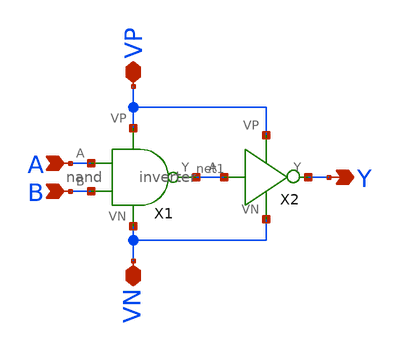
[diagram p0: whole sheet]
** sch_path: mp1/and/and.sch
**.subckt and A B VP VN Y
*.ipin A
*.ipin B
*.iopin VP
*.iopin VN
*.opin Y
X2 net1 Y VP VN inverter
X1 A B net1 VP VN nand
**.ends

* expanding   symbol:  /home/madvlsi/Documents/mp1/inverter/inverter.sym # of pins=4
** sym_path: mp1/inverter/inverter.sym
** sch_path: mp1/inverter/inverter.sch
.subckt inverter A Y VP VN
*.ipin A
*.iopin VP
*.iopin VN
*.opin Y
XM1 Y A VN VN sky130_fd_pr__nfet_01v8 L=0.15 W=1 nf=1 ad='int((nf+1)/2) * W/nf * 0.29' as='int((nf+2)/2) * W/nf * 0.29'
+ pd='2*int((nf+1)/2) * (W/nf + 0.29)' ps='2*int((nf+2)/2) * (W/nf + 0.29)' nrd='0.29 / W' nrs='0.29 / W'
+ sa=0 sb=0 sd=0 mult=1 m=1
XM2 Y A VP VP sky130_fd_pr__pfet_01v8 L=0.15 W=1 nf=1 ad='int((nf+1)/2) * W/nf * 0.29' as='int((nf+2)/2) * W/nf * 0.29'
+ pd='2*int((nf+1)/2) * (W/nf + 0.29)' ps='2*int((nf+2)/2) * (W/nf + 0.29)' nrd='0.29 / W' nrs='0.29 / W'
+ sa=0 sb=0 sd=0 mult=1 m=1
.ends


* expanding   symbol:  /home/madvlsi/Documents/mp1/nand/nand.sym # of pins=5
** sym_path: mp1/nand/nand.sym
** sch_path: mp1/nand/nand.sch
.subckt nand A B Y VP VN
*.ipin A
*.ipin B
*.opin Y
*.iopin VP
*.iopin VN
XM1 Y A VP VP sky130_fd_pr__pfet_01v8 L=0.15 W=1 nf=1 ad='int((nf+1)/2) * W/nf * 0.29' as='int((nf+2)/2) * W/nf * 0.29'
+ pd='2*int((nf+1)/2) * (W/nf + 0.29)' ps='2*int((nf+2)/2) * (W/nf + 0.29)' nrd='0.29 / W' nrs='0.29 / W'
+ sa=0 sb=0 sd=0 mult=1 m=1
XM2 Y B VP VP sky130_fd_pr__pfet_01v8 L=0.15 W=1 nf=1 ad='int((nf+1)/2) * W/nf * 0.29' as='int((nf+2)/2) * W/nf * 0.29'
+ pd='2*int((nf+1)/2) * (W/nf + 0.29)' ps='2*int((nf+2)/2) * (W/nf + 0.29)' nrd='0.29 / W' nrs='0.29 / W'
+ sa=0 sb=0 sd=0 mult=1 m=1
XM3 Y A net1 VN sky130_fd_pr__nfet_01v8 L=0.15 W=1 nf=1 ad='int((nf+1)/2) * W/nf * 0.29' as='int((nf+2)/2) * W/nf * 0.29'
+ pd='2*int((nf+1)/2) * (W/nf + 0.29)' ps='2*int((nf+2)/2) * (W/nf + 0.29)' nrd='0.29 / W' nrs='0.29 / W'
+ sa=0 sb=0 sd=0 mult=1 m=1
XM4 net1 B VN VN sky130_fd_pr__nfet_01v8 L=0.15 W=1 nf=1 ad='int((nf+1)/2) * W/nf * 0.29' as='int((nf+2)/2) * W/nf * 0.29'
+ pd='2*int((nf+1)/2) * (W/nf + 0.29)' ps='2*int((nf+2)/2) * (W/nf + 0.29)' nrd='0.29 / W' nrs='0.29 / W'
+ sa=0 sb=0 sd=0 mult=1 m=1
.ends

.end
